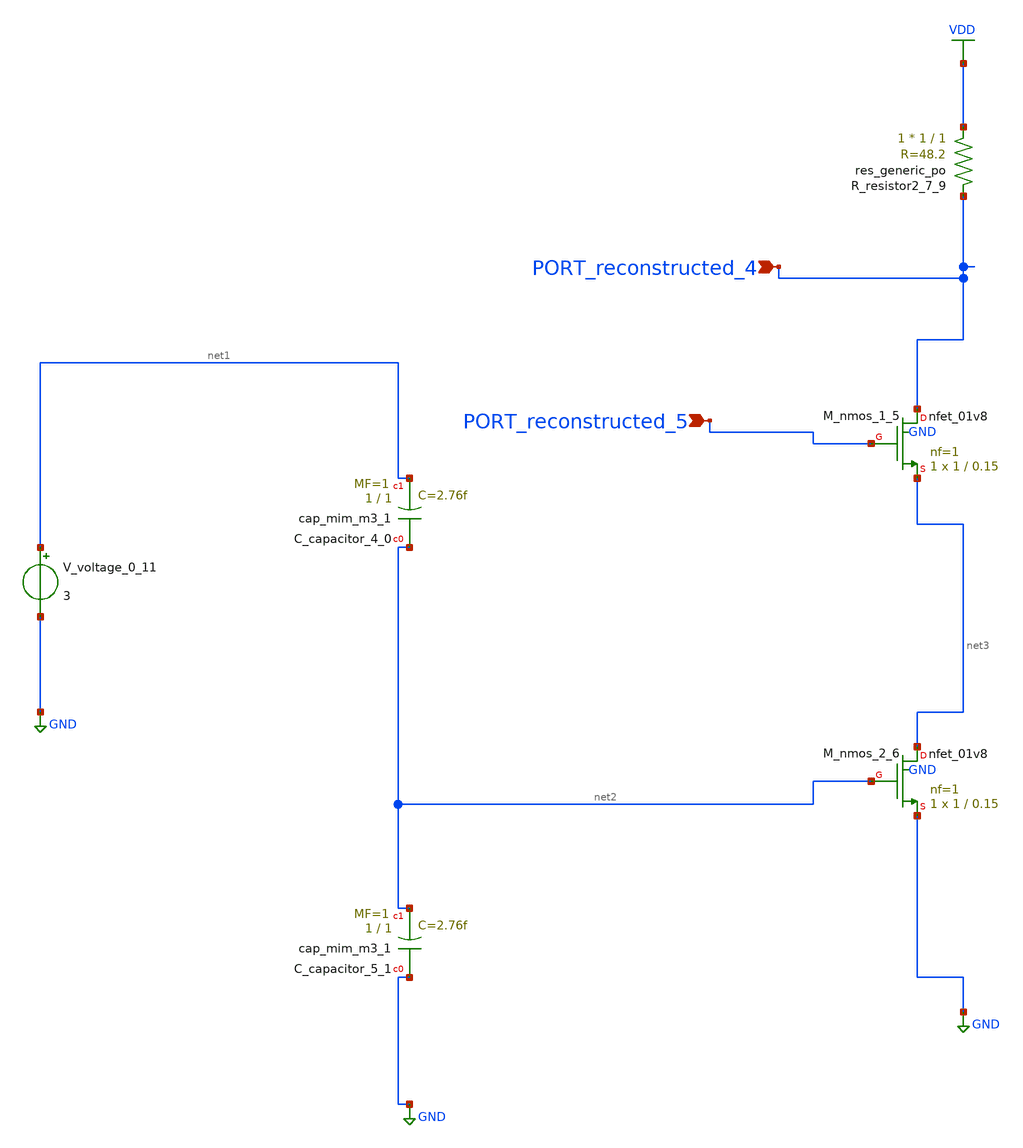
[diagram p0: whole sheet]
** sch_path: schematics/AMSNet/559.sch
**.subckt 559 PORT_reconstructed_4 PORT_reconstructed_5
*.ipin PORT_reconstructed_4
*.ipin PORT_reconstructed_5
XC_capacitor_4_0 net2 net1 sky130_fd_pr__cap_mim_m3_1 W=1 L=1 MF=1 m=1
XC_capacitor_5_1 GND net2 sky130_fd_pr__cap_mim_m3_1 W=1 L=1 MF=1 m=1
XM_nmos_1_5 PORT_reconstructed_4 PORT_reconstructed_5 net3 GND sky130_fd_pr__nfet_01v8 L=0.15 W=1 nf=1
+ ad='int((1 + 1)/2) * 1 / 1 * 0.29' as='int((1 + 2)/2) * 1 / 1 * 0.29' pd='2*int((1 + 1)/2) * (1 / 1 + 0.29)'
+ ps='2*int((1 + 2)/2) * (1 / 1 + 0.29)' nrd='0.29 / 1 ' nrs='0.29 / 1 ' sa=0 sb=0 sd=0 mult=1 m=1
XM_nmos_2_6 net3 net2 GND GND sky130_fd_pr__nfet_01v8 L=0.15 W=1 nf=1 ad='int((1 + 1)/2) * 1 / 1 * 0.29'
+ as='int((1 + 2)/2) * 1 / 1 * 0.29' pd='2*int((1 + 1)/2) * (1 / 1 + 0.29)' ps='2*int((1 + 2)/2) * (1 / 1 + 0.29)'
+ nrd='0.29 / 1 ' nrs='0.29 / 1 ' sa=0 sb=0 sd=0 mult=1 m=1
XR_resistor2_7_9 VDD PORT_reconstructed_4 sky130_fd_pr__res_generic_po W=1 L=1 m=1
V_voltage_0_11 net1 GND 3
**.ends
.GLOBAL GND
.GLOBAL VDD
.end
